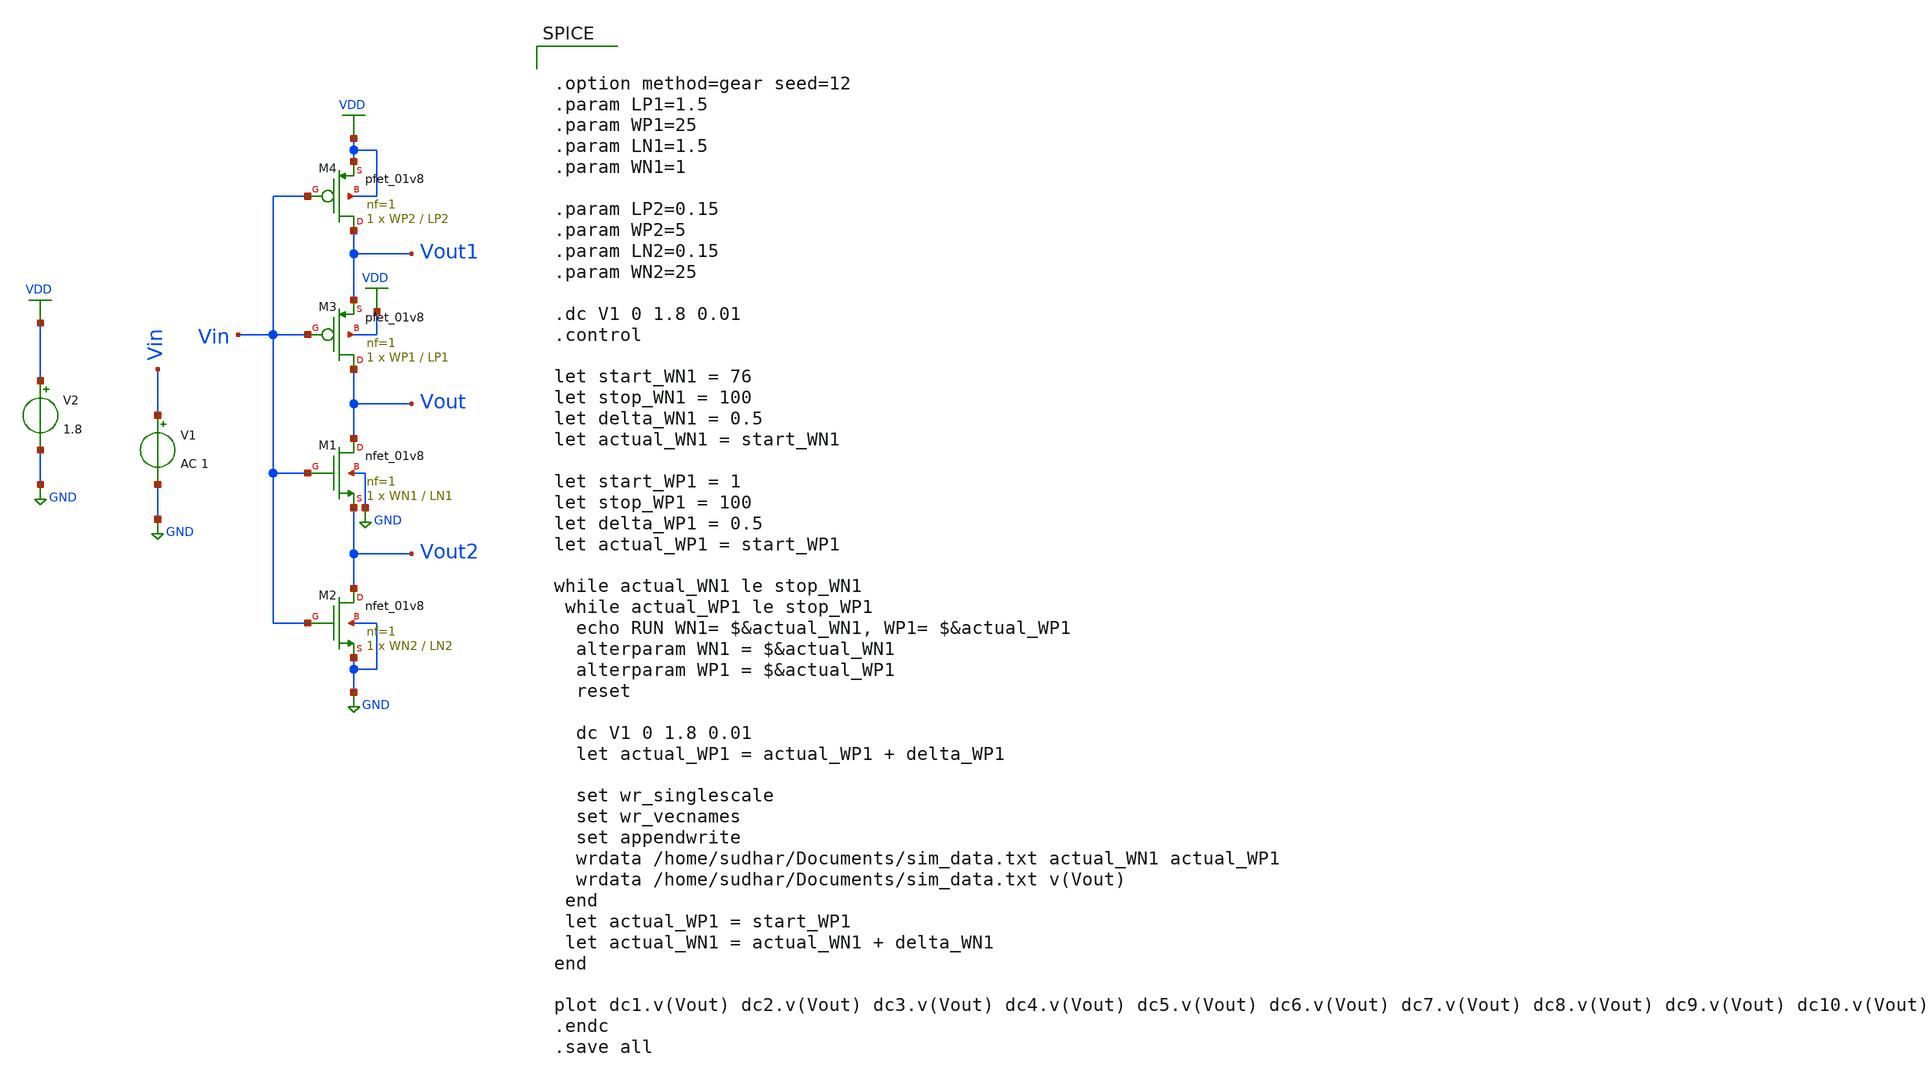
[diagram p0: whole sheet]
** sch_path: LIQAF circuit/Size Tuning/Size_Sweep.sch
**.subckt Size_Sweep
XM1 Vout Vin Vout2 GND sky130_fd_pr__nfet_01v8 L=LN1 W=WN1 nf=1 ad='int((nf+1)/2) * W/nf * 0.29' as='int((nf+2)/2) * W/nf * 0.29'
+ pd='2*int((nf+1)/2) * (W/nf + 0.29)' ps='2*int((nf+2)/2) * (W/nf + 0.29)' nrd='0.29 / W' nrs='0.29 / W'
+ sa=0 sb=0 sd=0 mult=1 m=1
V1 Vin GND AC 1
V2 VDD GND 1.8
XM2 Vout2 Vin GND GND sky130_fd_pr__nfet_01v8 L=LN2 W=WN2 nf=1 ad='int((nf+1)/2) * W/nf * 0.29' as='int((nf+2)/2) * W/nf * 0.29'
+ pd='2*int((nf+1)/2) * (W/nf + 0.29)' ps='2*int((nf+2)/2) * (W/nf + 0.29)' nrd='0.29 / W' nrs='0.29 / W'
+ sa=0 sb=0 sd=0 mult=1 m=1
XM3 Vout Vin Vout1 VDD sky130_fd_pr__pfet_01v8 L=LP1 W=WP1 nf=1 ad='int((nf+1)/2) * W/nf * 0.29' as='int((nf+2)/2) * W/nf * 0.29'
+ pd='2*int((nf+1)/2) * (W/nf + 0.29)' ps='2*int((nf+2)/2) * (W/nf + 0.29)' nrd='0.29 / W' nrs='0.29 / W'
+ sa=0 sb=0 sd=0 mult=1 m=1
XM4 Vout1 Vin VDD VDD sky130_fd_pr__pfet_01v8 L=LP2 W=WP2 nf=1 ad='int((nf+1)/2) * W/nf * 0.29' as='int((nf+2)/2) * W/nf * 0.29'
+ pd='2*int((nf+1)/2) * (W/nf + 0.29)' ps='2*int((nf+2)/2) * (W/nf + 0.29)' nrd='0.29 / W' nrs='0.29 / W'
+ sa=0 sb=0 sd=0 mult=1 m=1
**** begin user architecture code
 ** manual skywater pdks install (with patches applied)
* .lib $::SKYWATER_MODELS/models/sky130.lib.spice tt

** opencircuitdesign pdks install
.lib $::SKYWATER_MODELS/sky130.lib.spice tt

.param mc_mm_switch=0
.param mc_pr_switch=0
.param LP1=0.15



.option method=gear seed=12
.param LP1=1.5
.param WP1=25
.param LN1=1.5
.param WN1=1

.param LP2=0.15
.param WP2=5
.param LN2=0.15
.param WN2=25

.dc V1 0 1.8 0.01
.control

let start_WN1 = 76
let stop_WN1 = 100
let delta_WN1 = 0.5
let actual_WN1 = start_WN1

let start_WP1 = 1
let stop_WP1 = 100
let delta_WP1 = 0.5
let actual_WP1 = start_WP1

while actual_WN1 le stop_WN1
 while actual_WP1 le stop_WP1
  echo RUN WN1= $&actual_WN1, WP1= $&actual_WP1
  alterparam WN1 = $&actual_WN1
  alterparam WP1 = $&actual_WP1
  reset

  dc V1 0 1.8 0.01
  let actual_WP1 = actual_WP1 + delta_WP1

  set wr_singlescale
  set wr_vecnames
  set appendwrite
  wrdata /home/sudhar/Documents/sim_data.txt actual_WN1 actual_WP1
  wrdata /home/sudhar/Documents/sim_data.txt v(Vout)
 end
 let actual_WP1 = start_WP1
 let actual_WN1 = actual_WN1 + delta_WN1
end

plot dc1.v(Vout) dc2.v(Vout) dc3.v(Vout) dc4.v(Vout) dc5.v(Vout) dc6.v(Vout) dc7.v(Vout) dc8.v(Vout)
+ dc9.v(Vout) dc10.v(Vout)
.endc
.save all

**** end user architecture code
**.ends
.GLOBAL GND
.GLOBAL VDD
.end
